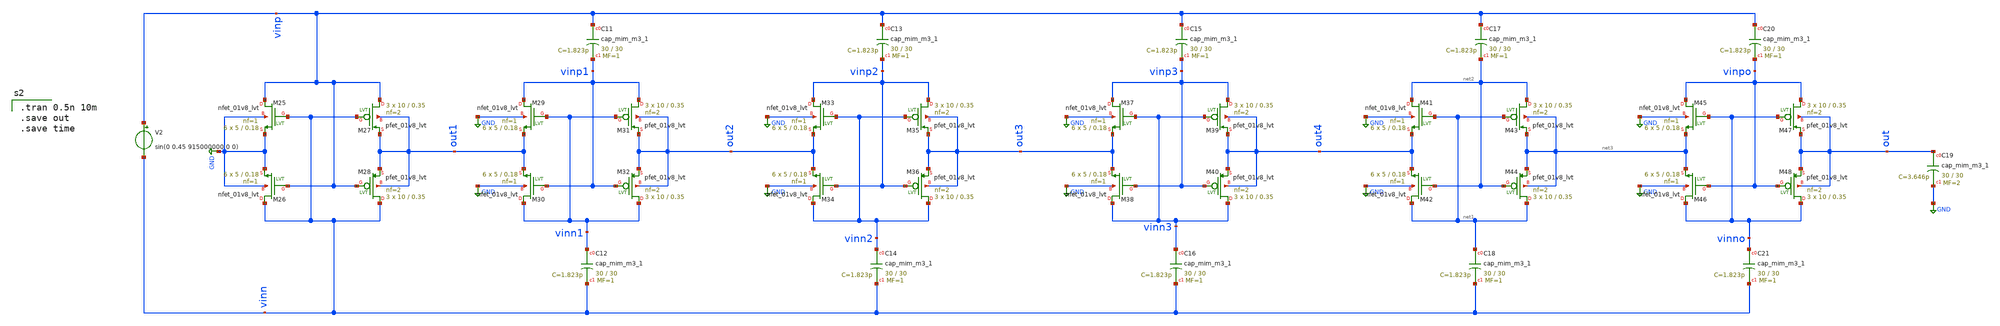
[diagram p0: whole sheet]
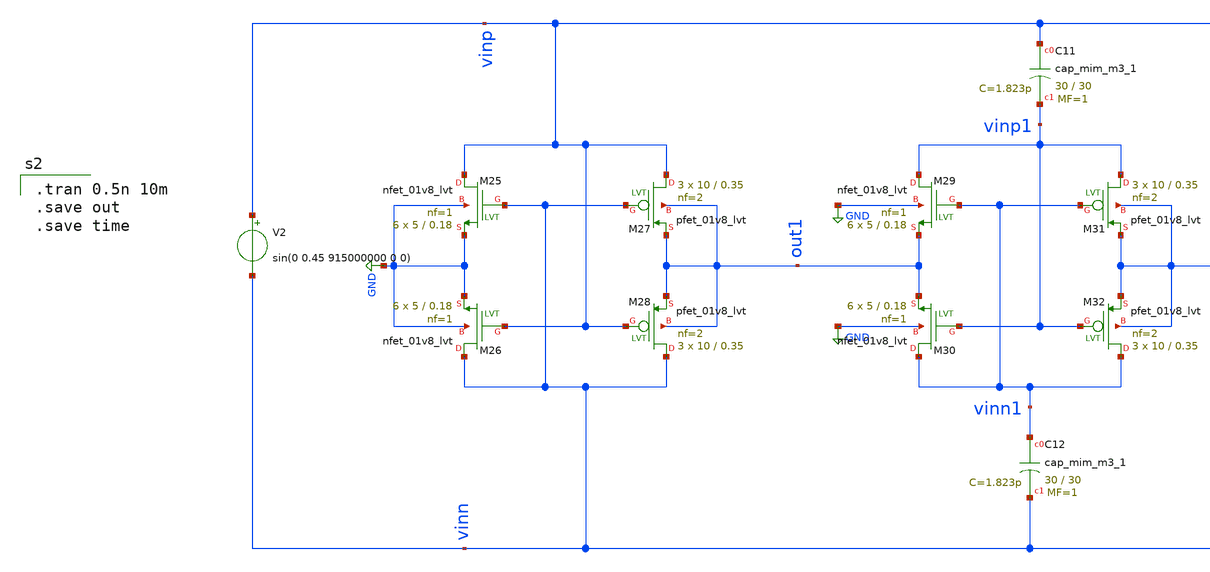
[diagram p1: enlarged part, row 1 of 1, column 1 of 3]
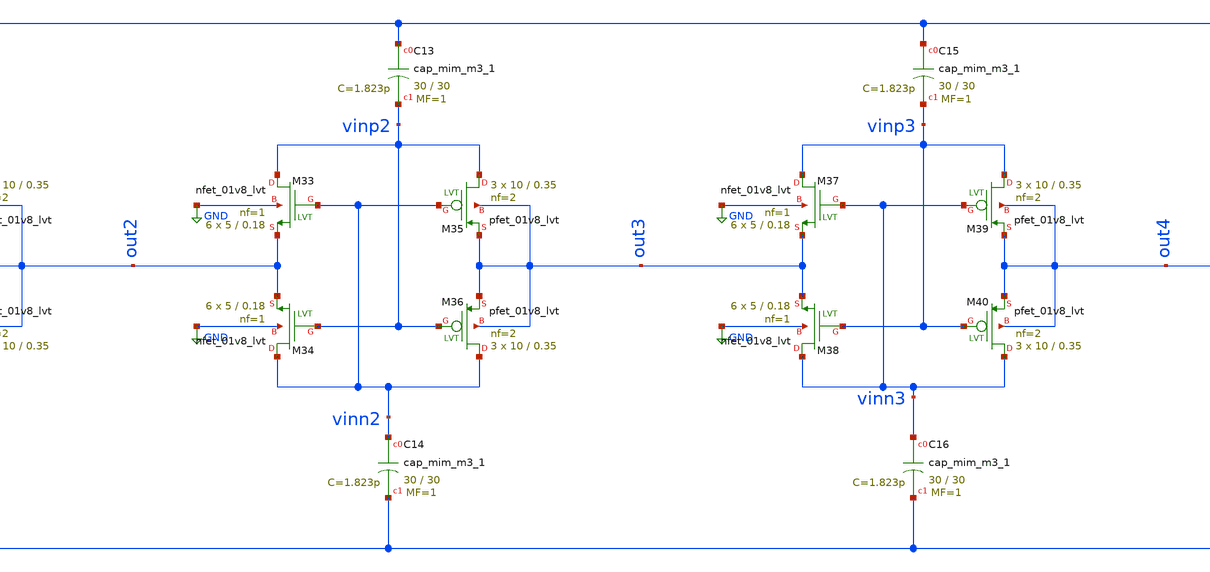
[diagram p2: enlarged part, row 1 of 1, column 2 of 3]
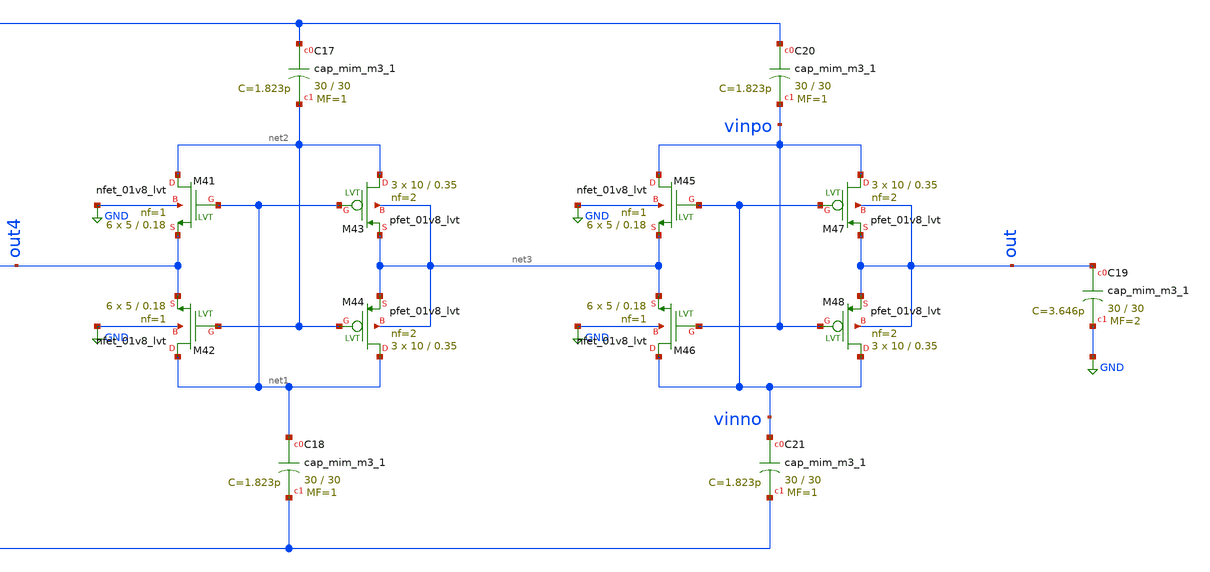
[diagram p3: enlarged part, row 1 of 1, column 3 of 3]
** sch_path: XSCHEM/rectifier_lvt_01v8_design_tb.sch
**.subckt rectifier_lvt_01v8_design_tb
V2 vinp vinn sin(0 0.45 915000000 0 0)
XC11 vinp vinp1 sky130_fd_pr__cap_mim_m3_1 W=30 L=30 MF=1 m=1
XC12 vinn1 vinn sky130_fd_pr__cap_mim_m3_1 W=30 L=30 MF=1 m=1
XC13 vinp vinp2 sky130_fd_pr__cap_mim_m3_1 W=30 L=30 MF=1 m=1
XC14 vinn2 vinn sky130_fd_pr__cap_mim_m3_1 W=30 L=30 MF=1 m=1
XM25 vinp vinn GND GND sky130_fd_pr__nfet_01v8_lvt L=0.18 W=5 nf=1 ad='int((nf+1)/2) * W/nf * 0.29' as='int((nf+2)/2) * W/nf * 0.29'
+ pd='2*int((nf+1)/2) * (W/nf + 0.29)' ps='2*int((nf+2)/2) * (W/nf + 0.29)' nrd='0.29 / W' nrs='0.29 / W'
+ sa=0 sb=0 sd=0 mult=6 m=6
XM26 vinn vinp GND GND sky130_fd_pr__nfet_01v8_lvt L=0.18 W=5 nf=1 ad='int((nf+1)/2) * W/nf * 0.29' as='int((nf+2)/2) * W/nf * 0.29'
+ pd='2*int((nf+1)/2) * (W/nf + 0.29)' ps='2*int((nf+2)/2) * (W/nf + 0.29)' nrd='0.29 / W' nrs='0.29 / W'
+ sa=0 sb=0 sd=0 mult=6 m=6
XM27 vinp vinn out1 out1 sky130_fd_pr__pfet_01v8_lvt L=0.35 W=10 nf=2 ad='int((nf+1)/2) * W/nf * 0.29'
+ as='int((nf+2)/2) * W/nf * 0.29' pd='2*int((nf+1)/2) * (W/nf + 0.29)' ps='2*int((nf+2)/2) * (W/nf + 0.29)'
+ nrd='0.29 / W' nrs='0.29 / W' sa=0 sb=0 sd=0 mult=3 m=3
XM28 vinn vinp out1 out1 sky130_fd_pr__pfet_01v8_lvt L=0.35 W=10 nf=2 ad='int((nf+1)/2) * W/nf * 0.29'
+ as='int((nf+2)/2) * W/nf * 0.29' pd='2*int((nf+1)/2) * (W/nf + 0.29)' ps='2*int((nf+2)/2) * (W/nf + 0.29)'
+ nrd='0.29 / W' nrs='0.29 / W' sa=0 sb=0 sd=0 mult=3 m=3
XM29 vinp1 vinn1 out1 GND sky130_fd_pr__nfet_01v8_lvt L=0.18 W=5 nf=1 ad='int((nf+1)/2) * W/nf * 0.29'
+ as='int((nf+2)/2) * W/nf * 0.29' pd='2*int((nf+1)/2) * (W/nf + 0.29)' ps='2*int((nf+2)/2) * (W/nf + 0.29)'
+ nrd='0.29 / W' nrs='0.29 / W' sa=0 sb=0 sd=0 mult=6 m=6
XM30 vinn1 vinp1 out1 GND sky130_fd_pr__nfet_01v8_lvt L=0.18 W=5 nf=1 ad='int((nf+1)/2) * W/nf * 0.29'
+ as='int((nf+2)/2) * W/nf * 0.29' pd='2*int((nf+1)/2) * (W/nf + 0.29)' ps='2*int((nf+2)/2) * (W/nf + 0.29)'
+ nrd='0.29 / W' nrs='0.29 / W' sa=0 sb=0 sd=0 mult=6 m=6
XM31 vinp1 vinn1 out2 out2 sky130_fd_pr__pfet_01v8_lvt L=0.35 W=10 nf=2 ad='int((nf+1)/2) * W/nf * 0.29'
+ as='int((nf+2)/2) * W/nf * 0.29' pd='2*int((nf+1)/2) * (W/nf + 0.29)' ps='2*int((nf+2)/2) * (W/nf + 0.29)'
+ nrd='0.29 / W' nrs='0.29 / W' sa=0 sb=0 sd=0 mult=3 m=3
XM32 vinn1 vinp1 out2 out2 sky130_fd_pr__pfet_01v8_lvt L=0.35 W=10 nf=2 ad='int((nf+1)/2) * W/nf * 0.29'
+ as='int((nf+2)/2) * W/nf * 0.29' pd='2*int((nf+1)/2) * (W/nf + 0.29)' ps='2*int((nf+2)/2) * (W/nf + 0.29)'
+ nrd='0.29 / W' nrs='0.29 / W' sa=0 sb=0 sd=0 mult=3 m=3
XM33 vinp2 vinn2 out2 GND sky130_fd_pr__nfet_01v8_lvt L=0.18 W=5 nf=1 ad='int((nf+1)/2) * W/nf * 0.29'
+ as='int((nf+2)/2) * W/nf * 0.29' pd='2*int((nf+1)/2) * (W/nf + 0.29)' ps='2*int((nf+2)/2) * (W/nf + 0.29)'
+ nrd='0.29 / W' nrs='0.29 / W' sa=0 sb=0 sd=0 mult=6 m=6
XM34 vinn2 vinp2 out2 GND sky130_fd_pr__nfet_01v8_lvt L=0.18 W=5 nf=1 ad='int((nf+1)/2) * W/nf * 0.29'
+ as='int((nf+2)/2) * W/nf * 0.29' pd='2*int((nf+1)/2) * (W/nf + 0.29)' ps='2*int((nf+2)/2) * (W/nf + 0.29)'
+ nrd='0.29 / W' nrs='0.29 / W' sa=0 sb=0 sd=0 mult=6 m=6
XM35 vinp2 vinn2 out3 out3 sky130_fd_pr__pfet_01v8_lvt L=0.35 W=10 nf=2 ad='int((nf+1)/2) * W/nf * 0.29'
+ as='int((nf+2)/2) * W/nf * 0.29' pd='2*int((nf+1)/2) * (W/nf + 0.29)' ps='2*int((nf+2)/2) * (W/nf + 0.29)'
+ nrd='0.29 / W' nrs='0.29 / W' sa=0 sb=0 sd=0 mult=3 m=3
XM36 vinn2 vinp2 out3 out3 sky130_fd_pr__pfet_01v8_lvt L=0.35 W=10 nf=2 ad='int((nf+1)/2) * W/nf * 0.29'
+ as='int((nf+2)/2) * W/nf * 0.29' pd='2*int((nf+1)/2) * (W/nf + 0.29)' ps='2*int((nf+2)/2) * (W/nf + 0.29)'
+ nrd='0.29 / W' nrs='0.29 / W' sa=0 sb=0 sd=0 mult=3 m=3
XC15 vinp vinp3 sky130_fd_pr__cap_mim_m3_1 W=30 L=30 MF=1 m=1
XC16 vinn3 vinn sky130_fd_pr__cap_mim_m3_1 W=30 L=30 MF=1 m=1
XM37 vinp3 vinn3 out3 GND sky130_fd_pr__nfet_01v8_lvt L=0.18 W=5 nf=1 ad='int((nf+1)/2) * W/nf * 0.29'
+ as='int((nf+2)/2) * W/nf * 0.29' pd='2*int((nf+1)/2) * (W/nf + 0.29)' ps='2*int((nf+2)/2) * (W/nf + 0.29)'
+ nrd='0.29 / W' nrs='0.29 / W' sa=0 sb=0 sd=0 mult=6 m=6
XM38 vinn3 vinp3 out3 GND sky130_fd_pr__nfet_01v8_lvt L=0.18 W=5 nf=1 ad='int((nf+1)/2) * W/nf * 0.29'
+ as='int((nf+2)/2) * W/nf * 0.29' pd='2*int((nf+1)/2) * (W/nf + 0.29)' ps='2*int((nf+2)/2) * (W/nf + 0.29)'
+ nrd='0.29 / W' nrs='0.29 / W' sa=0 sb=0 sd=0 mult=6 m=6
XM39 vinp3 vinn3 out4 out4 sky130_fd_pr__pfet_01v8_lvt L=0.35 W=10 nf=2 ad='int((nf+1)/2) * W/nf * 0.29'
+ as='int((nf+2)/2) * W/nf * 0.29' pd='2*int((nf+1)/2) * (W/nf + 0.29)' ps='2*int((nf+2)/2) * (W/nf + 0.29)'
+ nrd='0.29 / W' nrs='0.29 / W' sa=0 sb=0 sd=0 mult=3 m=3
XM40 vinn3 vinp3 out4 out4 sky130_fd_pr__pfet_01v8_lvt L=0.35 W=10 nf=2 ad='int((nf+1)/2) * W/nf * 0.29'
+ as='int((nf+2)/2) * W/nf * 0.29' pd='2*int((nf+1)/2) * (W/nf + 0.29)' ps='2*int((nf+2)/2) * (W/nf + 0.29)'
+ nrd='0.29 / W' nrs='0.29 / W' sa=0 sb=0 sd=0 mult=3 m=3
XC17 vinp net2 sky130_fd_pr__cap_mim_m3_1 W=30 L=30 MF=1 m=1
XC18 net1 vinn sky130_fd_pr__cap_mim_m3_1 W=30 L=30 MF=1 m=1
XM41 net2 net1 out4 GND sky130_fd_pr__nfet_01v8_lvt L=0.18 W=5 nf=1 ad='int((nf+1)/2) * W/nf * 0.29'
+ as='int((nf+2)/2) * W/nf * 0.29' pd='2*int((nf+1)/2) * (W/nf + 0.29)' ps='2*int((nf+2)/2) * (W/nf + 0.29)'
+ nrd='0.29 / W' nrs='0.29 / W' sa=0 sb=0 sd=0 mult=6 m=6
XM42 net1 net2 out4 GND sky130_fd_pr__nfet_01v8_lvt L=0.18 W=5 nf=1 ad='int((nf+1)/2) * W/nf * 0.29'
+ as='int((nf+2)/2) * W/nf * 0.29' pd='2*int((nf+1)/2) * (W/nf + 0.29)' ps='2*int((nf+2)/2) * (W/nf + 0.29)'
+ nrd='0.29 / W' nrs='0.29 / W' sa=0 sb=0 sd=0 mult=6 m=6
XM43 net2 net1 net3 net3 sky130_fd_pr__pfet_01v8_lvt L=0.35 W=10 nf=2 ad='int((nf+1)/2) * W/nf * 0.29'
+ as='int((nf+2)/2) * W/nf * 0.29' pd='2*int((nf+1)/2) * (W/nf + 0.29)' ps='2*int((nf+2)/2) * (W/nf + 0.29)'
+ nrd='0.29 / W' nrs='0.29 / W' sa=0 sb=0 sd=0 mult=3 m=3
XM44 net1 net2 net3 net3 sky130_fd_pr__pfet_01v8_lvt L=0.35 W=10 nf=2 ad='int((nf+1)/2) * W/nf * 0.29'
+ as='int((nf+2)/2) * W/nf * 0.29' pd='2*int((nf+1)/2) * (W/nf + 0.29)' ps='2*int((nf+2)/2) * (W/nf + 0.29)'
+ nrd='0.29 / W' nrs='0.29 / W' sa=0 sb=0 sd=0 mult=3 m=3
XC19 out GND sky130_fd_pr__cap_mim_m3_1 W=30 L=30 MF=2 m=2
XC20 vinp vinpo sky130_fd_pr__cap_mim_m3_1 W=30 L=30 MF=1 m=1
XC21 vinno vinn sky130_fd_pr__cap_mim_m3_1 W=30 L=30 MF=1 m=1
XM45 vinpo vinno net3 GND sky130_fd_pr__nfet_01v8_lvt L=0.18 W=5 nf=1 ad='int((nf+1)/2) * W/nf * 0.29'
+ as='int((nf+2)/2) * W/nf * 0.29' pd='2*int((nf+1)/2) * (W/nf + 0.29)' ps='2*int((nf+2)/2) * (W/nf + 0.29)'
+ nrd='0.29 / W' nrs='0.29 / W' sa=0 sb=0 sd=0 mult=6 m=6
XM46 vinno vinpo net3 GND sky130_fd_pr__nfet_01v8_lvt L=0.18 W=5 nf=1 ad='int((nf+1)/2) * W/nf * 0.29'
+ as='int((nf+2)/2) * W/nf * 0.29' pd='2*int((nf+1)/2) * (W/nf + 0.29)' ps='2*int((nf+2)/2) * (W/nf + 0.29)'
+ nrd='0.29 / W' nrs='0.29 / W' sa=0 sb=0 sd=0 mult=6 m=6
XM47 vinpo vinno out out sky130_fd_pr__pfet_01v8_lvt L=0.35 W=10 nf=2 ad='int((nf+1)/2) * W/nf * 0.29'
+ as='int((nf+2)/2) * W/nf * 0.29' pd='2*int((nf+1)/2) * (W/nf + 0.29)' ps='2*int((nf+2)/2) * (W/nf + 0.29)'
+ nrd='0.29 / W' nrs='0.29 / W' sa=0 sb=0 sd=0 mult=3 m=3
XM48 vinno vinpo out out sky130_fd_pr__pfet_01v8_lvt L=0.35 W=10 nf=2 ad='int((nf+1)/2) * W/nf * 0.29'
+ as='int((nf+2)/2) * W/nf * 0.29' pd='2*int((nf+1)/2) * (W/nf + 0.29)' ps='2*int((nf+2)/2) * (W/nf + 0.29)'
+ nrd='0.29 / W' nrs='0.29 / W' sa=0 sb=0 sd=0 mult=3 m=3
**** begin user architecture code

.tran 0.5n 10m
.save out
.save time


** opencircuitdesign pdks install
.lib $::SKYWATER_MODELS/sky130.lib.spice hh


**** end user architecture code
**.ends
.GLOBAL GND
.end
